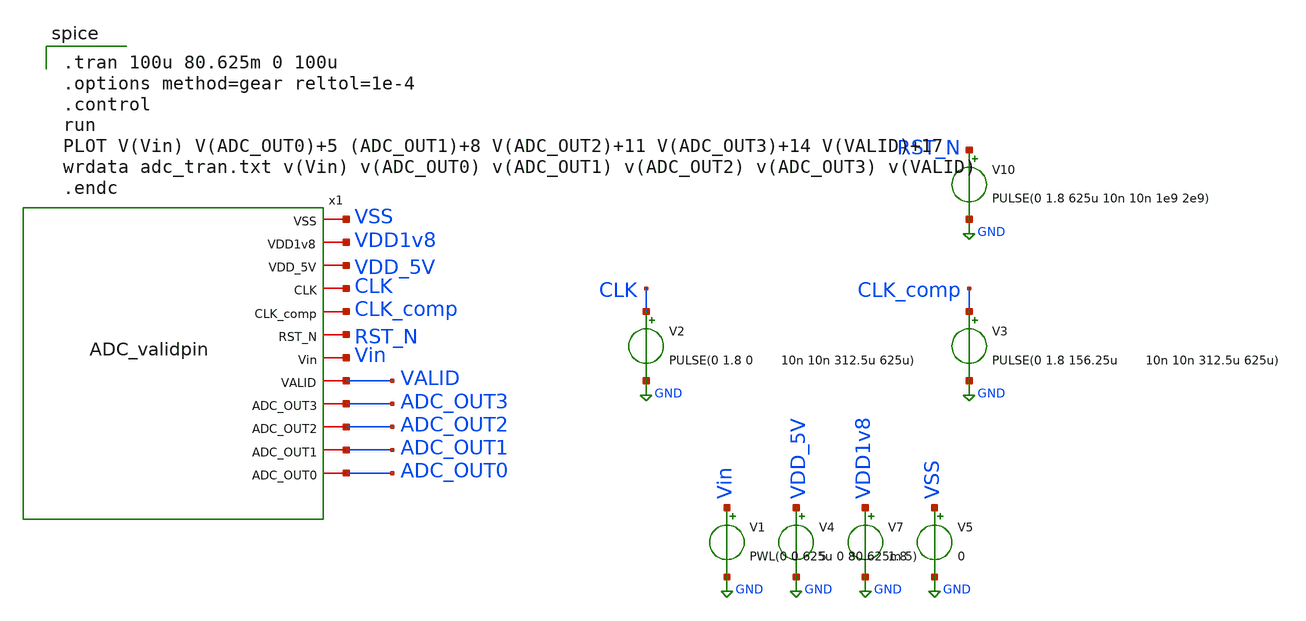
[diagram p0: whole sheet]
** sch_path: ADC/4bit_C2C/MagicAndSpice/ADC_validpin_TB.sch
**.subckt ADC_validpin_TB
x1 VSS VDD1v8 VDD_5V CLK CLK_comp RST_N Vin VALID ADC_OUT3 ADC_OUT2 ADC_OUT1 ADC_OUT0 ADC_validpin
V2 CLK GND PULSE(0 1.8 0 10n 10n 312.5u 625u)
V3 CLK_comp GND PULSE(0 1.8 156.25u 10n 10n 312.5u 625u)
V1 Vin GND PWL(0 0 625u 0 80.625m 5)
V4 VDD_5V GND 5
V7 VDD1v8 GND 1.8
V5 VSS GND 0
V10 RST_N GND PULSE(0 1.8 625u 10n 10n 1e9 2e9)
**** begin user architecture code

** opencircuitdesign pdks install
.lib $::SKYWATER_MODELS/sky130.lib.spice tt



.tran 100u 80.625m 0 100u
.options method=gear reltol=1e-4
.control
run
PLOT V(Vin) V(ADC_OUT0)+5 (ADC_OUT1)+8 V(ADC_OUT2)+11 V(ADC_OUT3)+14 V(VALID)+17
wrdata adc_tran.txt v(Vin) v(ADC_OUT0) v(ADC_OUT1) v(ADC_OUT2) v(ADC_OUT3) v(VALID)
.endc

**** end user architecture code
**.ends
.GLOBAL GND
.end
